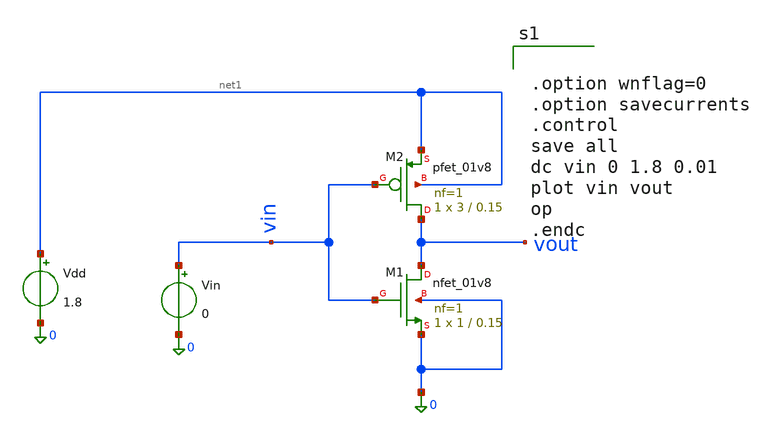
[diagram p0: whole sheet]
** sch_path: assignment.sch
**.subckt assignment
Vin vin 0 0
Vdd net1 0 1.8
XM2 vout vin net1 net1 sky130_fd_pr__pfet_01v8 L=0.15 W=3 nf=1 ad='int((1 + 1)/2) * 3 / 1 * 0.29' as='int((1 + 2)/2) * 3 / 1 * 0.29'
+ pd='2*int((1 + 1)/2) * (3 / 1 + 0.29)' ps='2*int((1 + 2)/2) * (3 / 1 + 0.29)' nrd='0.29 / 3 ' nrs='0.29 / 3 '
+ sa=0 sb=0 sd=0 mult=1 m=1
XM1 vout vin 0 0 sky130_fd_pr__nfet_01v8 L=0.15 W=1 nf=1 ad='int((1 + 1)/2) * 1 / 1 * 0.29' as='int((1 + 2)/2) * 1 / 1 * 0.29'
+ pd='2*int((1 + 1)/2) * (1 / 1 + 0.29)' ps='2*int((1 + 2)/2) * (1 / 1 + 0.29)' nrd='0.29 / 1 ' nrs='0.29 / 1 '
+ sa=0 sb=0 sd=0 mult=1 m=1
**** begin user architecture code


.option wnflag=0
.option savecurrents
.control
save all
dc vin 0 1.8 0.01
plot vin vout
op
.endc


 .lib /usr/local/share/pdk/sky130A/libs.tech/ngspice/sky130.lib.spice tt
.param_mc_mm_switch=0
.param_mc_pr_switch=1

**** end user architecture code
**.ends
.end
